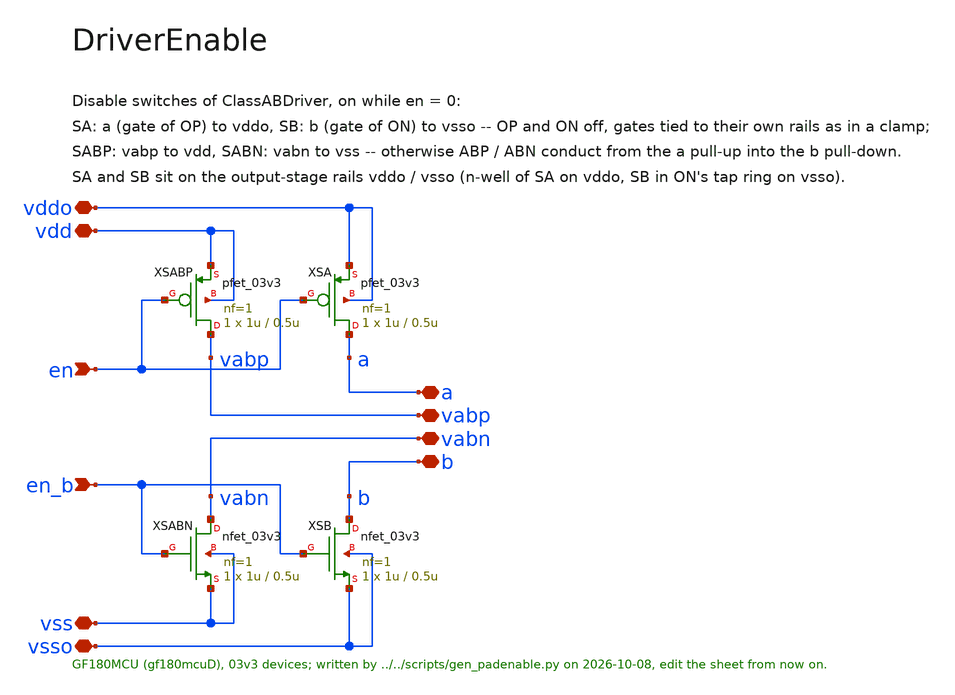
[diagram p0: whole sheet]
** sch_path: macros/PadEnable/schematic/xschem/DriverEnable.sch
**.subckt DriverEnable vdd vss vddo vsso en en_b a b vabp vabn
*.iopin vdd
*.iopin vss
*.iopin vddo
*.iopin vsso
*.ipin en
*.ipin en_b
*.iopin a
*.iopin b
*.iopin vabp
*.iopin vabn
XSA a en vddo vddo pfet_03v3 L=0.5u W=1u nf=1 ad='int((nf+1)/2) * W/nf * 0.18u' as='int((nf+2)/2) * W/nf * 0.18u'
+ pd='2*int((nf+1)/2) * (W/nf + 0.18u)' ps='2*int((nf+2)/2) * (W/nf + 0.18u)' nrd='0.18u / W' nrs='0.18u / W'
+ sa=0 sb=0 sd=0 m=1
XSABP vabp en vdd vdd pfet_03v3 L=0.5u W=1u nf=1 ad='int((nf+1)/2) * W/nf * 0.18u' as='int((nf+2)/2) * W/nf * 0.18u'
+ pd='2*int((nf+1)/2) * (W/nf + 0.18u)' ps='2*int((nf+2)/2) * (W/nf + 0.18u)' nrd='0.18u / W' nrs='0.18u / W'
+ sa=0 sb=0 sd=0 m=1
XSB b en_b vsso vsso nfet_03v3 L=0.5u W=1u nf=1 ad='int((nf+1)/2) * W/nf * 0.18u' as='int((nf+2)/2) * W/nf * 0.18u'
+ pd='2*int((nf+1)/2) * (W/nf + 0.18u)' ps='2*int((nf+2)/2) * (W/nf + 0.18u)' nrd='0.18u / W' nrs='0.18u / W'
+ sa=0 sb=0 sd=0 m=1
XSABN vabn en_b vss vss nfet_03v3 L=0.5u W=1u nf=1 ad='int((nf+1)/2) * W/nf * 0.18u' as='int((nf+2)/2) * W/nf * 0.18u'
+ pd='2*int((nf+1)/2) * (W/nf + 0.18u)' ps='2*int((nf+2)/2) * (W/nf + 0.18u)' nrd='0.18u / W' nrs='0.18u / W'
+ sa=0 sb=0 sd=0 m=1
**.ends
.end
